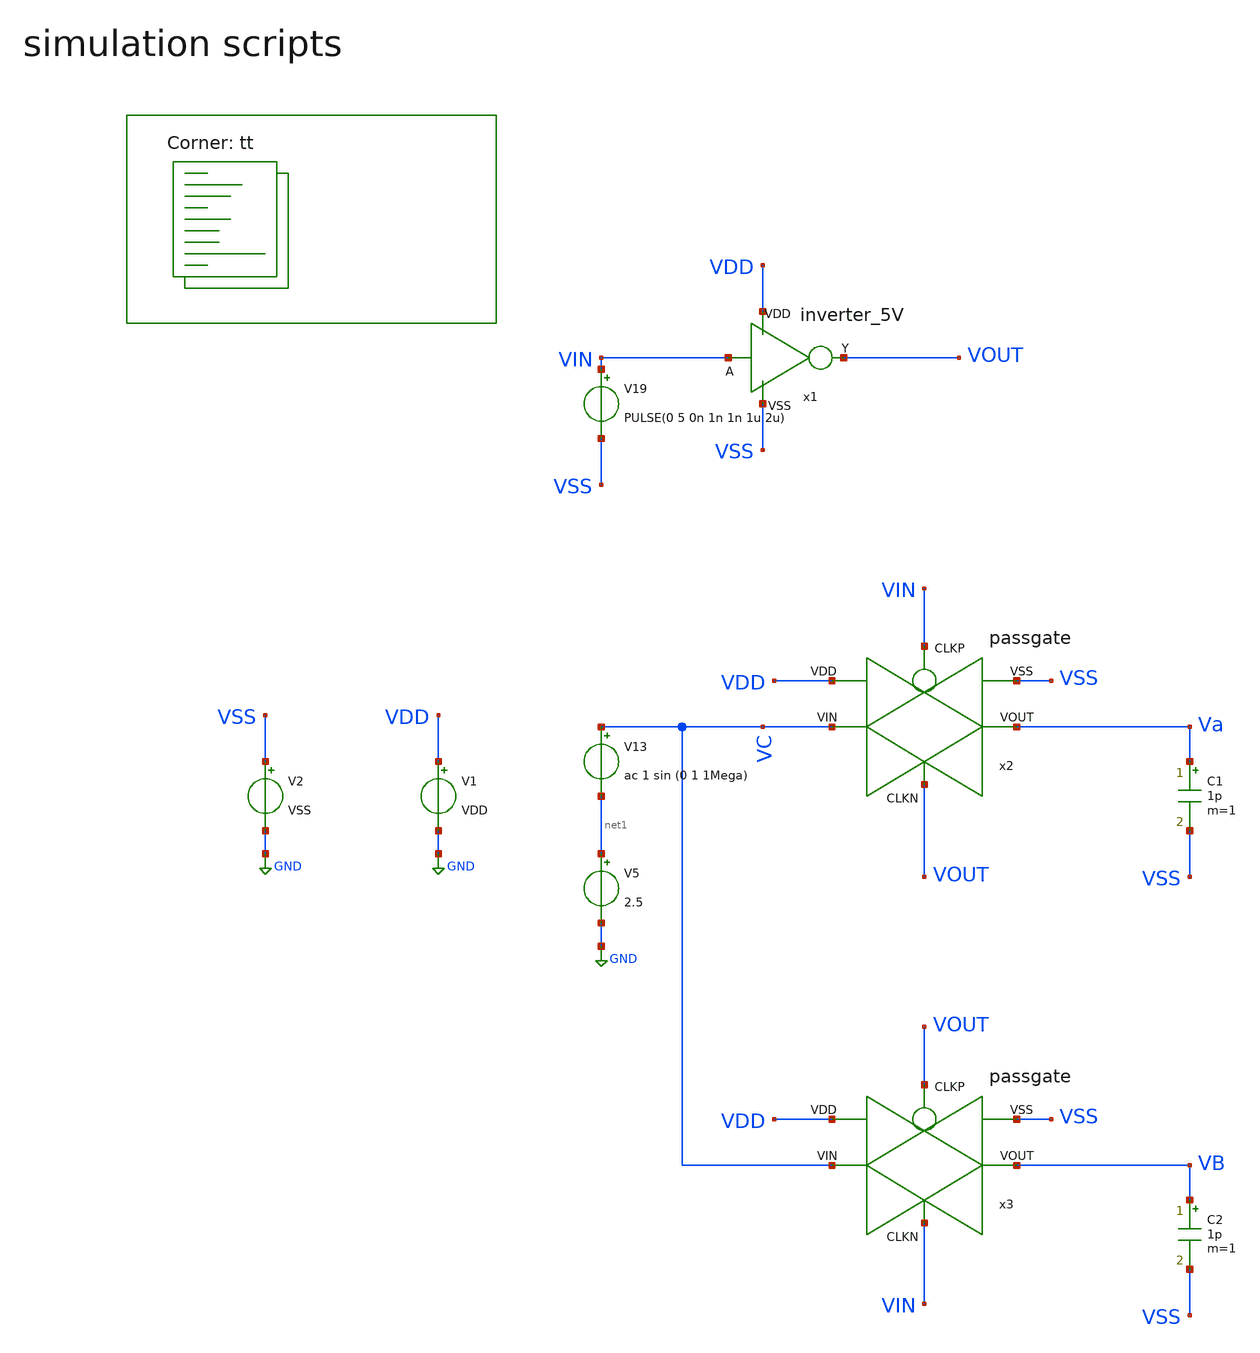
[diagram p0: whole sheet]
** sch_path: Learning/complex_projects/A_Two-Stage_Time_Division_Multiplexing_AFE_with_Input_Impedance_Boosting_DDA_for_EEG_Signal_Acquisition/sky130A_5V/input_buffer_chopper/pass_gate.sch
**.subckt pass_gate
V1 VDD GND VDD
V2 VSS GND VSS
x1 VDD VSS VIN VOUT inverter_5V
V19 VIN VSS PULSE(0 5 0n 1n 1n 1u 2u)
x2 VDD VSS VC Va VIN VOUT passgate
V5 net1 GND 2.5
V13 VC net1 ac 1 sin (0 1 1Mega)
C1 Va VSS 1p m=1
x3 VDD VSS VC VB VOUT VIN passgate
C2 VB VSS 1p m=1
**** begin user architecture code
.lib $::SKYWATER_MODELS/sky130.lib.spice tt

.Temp 27
.param VDD = 5
.param VCM = 2
.param V_ref = 1.2
.param VSS = 0
.param CL = 3p


.control

	save all
	tran 100p 10u

	plot v(VIN) v(VOUT)

	plot v(VC) v(Va) v(VB)

.endc


**** end user architecture code
**.ends

* expanding   symbol:  Sky130A/digital/inverter_5V.sym # of pins=4
** sym_path: LIB/Sky130A/digital/inverter_5V.sym
** sch_path: LIB/Sky130A/digital/inverter_5V.sch
.subckt inverter_5V VDD VSS A Y
*.iopin VDD
*.iopin VSS
*.iopin A
*.iopin Y
XM1 Y A VDD VDD sky130_fd_pr__pfet_g5v0d10v5 L=0.5 W='1 * 3 ' nf=3 ad='int((3 + 1)/2) * 1 * 0.29' as='int((3 + 2)/2) * 1 * 0.29'
+ pd='2*int((3 + 1)/2) * (1 + 0.29)' ps='2*int((3 + 2)/2) * (1 + 0.29)' nrd='0.29 / 1 / 3 ' nrs='0.29 / 1 / 3 '
+ sa=0 sb=0 sd=0 mult=1 m=1
XM2 Y A VSS VSS sky130_fd_pr__nfet_g5v0d10v5 L=0.5 W='1 * 1 ' nf=1 ad='int((nf+1)/2) * W / nf * 0.29'
+ as='int((nf+2)/2) * W / nf * 0.29' pd='2*int((nf+1)/2) * (W / nf + 0.29)' ps='2*int((nf+2)/2) * (W / nf + 0.29)'
+ nrd='0.29 / W ' nrs='0.29 / W ' sa=0 sb=0 sd=0 mult=1 m=1
.ends


* expanding   symbol:  Sky130A/switches/passgate.sym # of pins=6
** sym_path: LIB/Sky130A/switches/passgate.sym
** sch_path: LIB/Sky130A/switches/passgate.sch
.subckt passgate VDD VSS VIN VOUT CLKP CLKN
*.iopin VDD
*.iopin VSS
*.iopin VIN
*.iopin VOUT
*.iopin CLKP
*.iopin CLKN
XM1 VIN CLKP VOUT VDD sky130_fd_pr__pfet_g5v0d10v5 L=0.5 W='1 * 3 ' nf=3 ad='int((3 + 1)/2) * 1 * 0.29'
+ as='int((3 + 2)/2) * 1 * 0.29' pd='2*int((3 + 1)/2) * (1 + 0.29)' ps='2*int((3 + 2)/2) * (1 + 0.29)'
+ nrd='0.29 / 1 / 3 ' nrs='0.29 / 1 / 3 ' sa=0 sb=0 sd=0 mult=1 m=1
XM37 VIN CLKN VOUT VSS sky130_fd_pr__nfet_g5v0d10v5 L=0.5 W='1 * 1 ' nf=1 ad='int((nf+1)/2) * W / nf * 0.29'
+ as='int((nf+2)/2) * W / nf * 0.29' pd='2*int((nf+1)/2) * (W / nf + 0.29)' ps='2*int((nf+2)/2) * (W / nf + 0.29)'
+ nrd='0.29 / W ' nrs='0.29 / W ' sa=0 sb=0 sd=0 mult=1 m=1
.ends

.GLOBAL GND
.end
